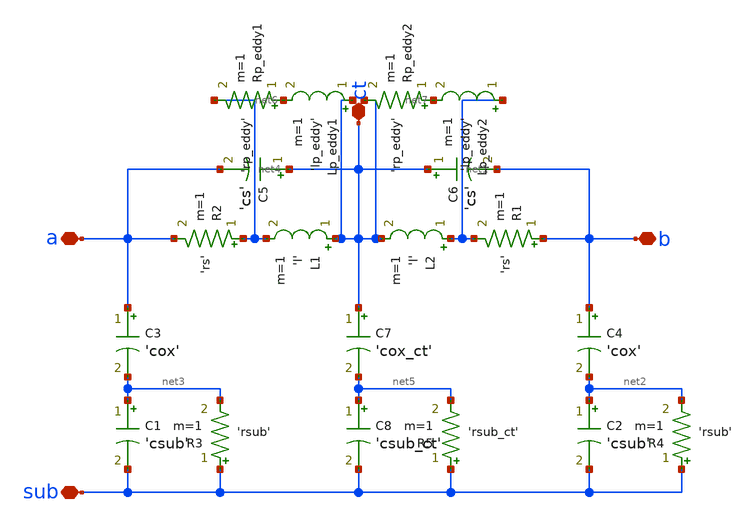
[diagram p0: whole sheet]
** sch_path: sch/inductor/inductor_spiral_diff.sch
**.subckt inductor_spiral_diff ct a b sub
*.iopin ct
*.iopin a
*.iopin b
*.iopin sub
C1 net3 sub 'csub' m=1
C2 net2 sub 'csub' m=1
L1 ct net4 'l' m=1
L2 net1 ct 'l' m=1
R1 b net1 'rs' m=1
R2 net4 a 'rs' m=1
R3 sub net3 'rsub' m=1
R4 sub net2 'rsub' m=1
C3 a net3 'cox' m=1
C4 b net2 'cox' m=1
C5 ct a 'cs' m=1
C6 ct b 'cs' m=1
C7 ct net5 'cox_ct' m=1
C8 net5 sub 'csub_ct' m=1
R5 sub net5 'rsub_ct' m=1
Rp_eddy1 net6 net4 'rp_eddy' m=1
Lp_eddy1 ct net6 'lp_eddy' m=1
Rp_eddy2 net7 ct 'rp_eddy' m=1
Lp_eddy2 net1 net7 'lp_eddy' m=1
**** begin user architecture code


K1 L1 L2 'k_coupling'


**** end user architecture code
**.ends
.end
